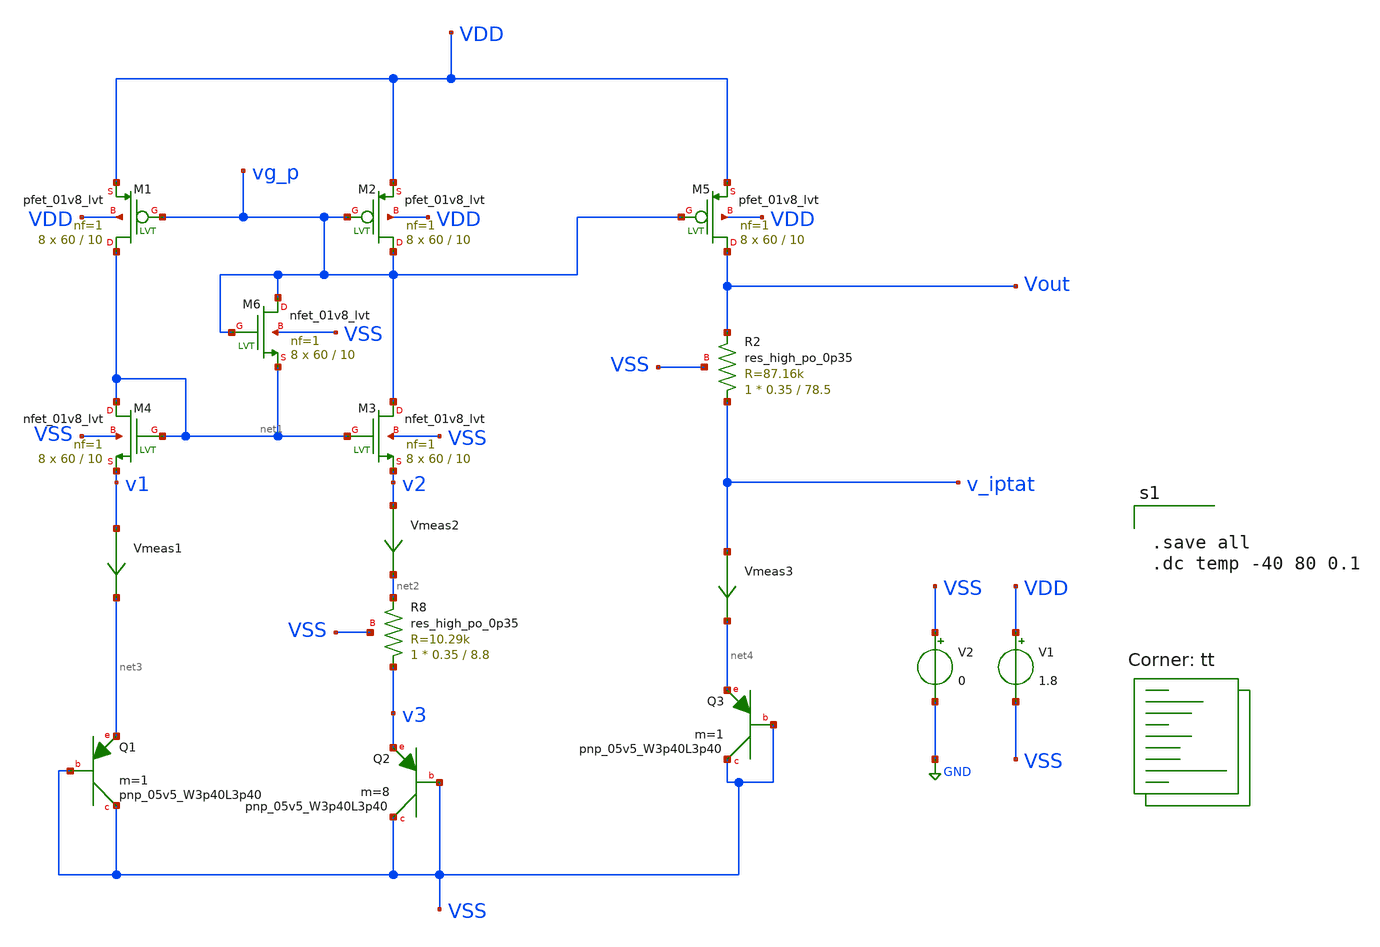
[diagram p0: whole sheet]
** sch_path: xschem/bandgap.sch
**.subckt bandgap
XQ1 VSS VSS net3 sky130_fd_pr__pnp_05v5_W3p40L3p40 m=1
V1 VDD VSS 1.8
XQ3 VSS VSS net4 sky130_fd_pr__pnp_05v5_W3p40L3p40 m=1
XQ2 VSS VSS v3 sky130_fd_pr__pnp_05v5_W3p40L3p40 m=8
V2 VSS GND 0
Vmeas1 v1 net3 0
.save i(vmeas1)
Vmeas2 v2 net2 0
.save i(vmeas2)
Vmeas3 v_iptat net4 0
.save i(vmeas3)
XM1 net1 vg_p VDD VDD sky130_fd_pr__pfet_01v8_lvt L=10 W=60 nf=1 ad='int((nf+1)/2) * W/nf * 0.29' as='int((nf+2)/2) * W/nf * 0.29'
+ pd='2*int((nf+1)/2) * (W/nf + 0.29)' ps='2*int((nf+2)/2) * (W/nf + 0.29)' nrd='0.29 / W' nrs='0.29 / W'
+ sa=0 sb=0 sd=0 mult=8 m=8
XM2 vg_p vg_p VDD VDD sky130_fd_pr__pfet_01v8_lvt L=10 W=60 nf=1 ad='int((nf+1)/2) * W/nf * 0.29' as='int((nf+2)/2) * W/nf * 0.29'
+ pd='2*int((nf+1)/2) * (W/nf + 0.29)' ps='2*int((nf+2)/2) * (W/nf + 0.29)' nrd='0.29 / W' nrs='0.29 / W'
+ sa=0 sb=0 sd=0 mult=8 m=8
XM5 Vout vg_p VDD VDD sky130_fd_pr__pfet_01v8_lvt L=10 W=60 nf=1 ad='int((nf+1)/2) * W/nf * 0.29' as='int((nf+2)/2) * W/nf * 0.29'
+ pd='2*int((nf+1)/2) * (W/nf + 0.29)' ps='2*int((nf+2)/2) * (W/nf + 0.29)' nrd='0.29 / W' nrs='0.29 / W'
+ sa=0 sb=0 sd=0 mult=8 m=8
XM6 vg_p vg_p net1 VSS sky130_fd_pr__nfet_01v8_lvt L=10 W=60 nf=1 ad='int((nf+1)/2) * W/nf * 0.29' as='int((nf+2)/2) * W/nf * 0.29'
+ pd='2*int((nf+1)/2) * (W/nf + 0.29)' ps='2*int((nf+2)/2) * (W/nf + 0.29)' nrd='0.29 / W' nrs='0.29 / W'
+ sa=0 sb=0 sd=0 mult=8 m=8
XM3 vg_p net1 v2 VSS sky130_fd_pr__nfet_01v8_lvt L=10 W=60 nf=1 ad='int((nf+1)/2) * W/nf * 0.29' as='int((nf+2)/2) * W/nf * 0.29'
+ pd='2*int((nf+1)/2) * (W/nf + 0.29)' ps='2*int((nf+2)/2) * (W/nf + 0.29)' nrd='0.29 / W' nrs='0.29 / W'
+ sa=0 sb=0 sd=0 mult=8 m=8
XM4 net1 net1 v1 VSS sky130_fd_pr__nfet_01v8_lvt L=10 W=60 nf=1 ad='int((nf+1)/2) * W/nf * 0.29' as='int((nf+2)/2) * W/nf * 0.29'
+ pd='2*int((nf+1)/2) * (W/nf + 0.29)' ps='2*int((nf+2)/2) * (W/nf + 0.29)' nrd='0.29 / W' nrs='0.29 / W'
+ sa=0 sb=0 sd=0 mult=8 m=8
XR8 v3 net2 VSS sky130_fd_pr__res_high_po_0p35 L=8.8 mult=1 m=1
XR2 v_iptat Vout VSS sky130_fd_pr__res_high_po_0p35 L=78.5 mult=1 m=1
**** begin user architecture code
.lib $::SKYWATER_MODELS/sky130.lib.spice tt


.save all
.dc temp -40 80 0.1


**** end user architecture code
**.ends
.GLOBAL GND
.end
